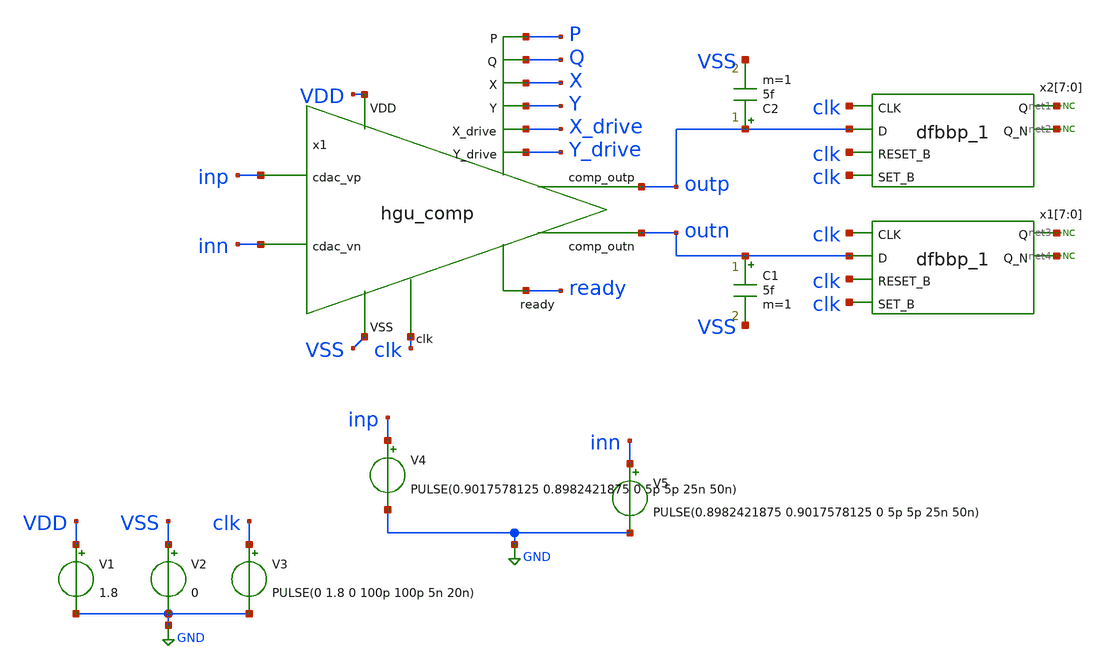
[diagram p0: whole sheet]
** sch_path: hgu/tb/tb_hgu_comp_withc.sch
**.subckt tb_hgu_comp_withc
x1 Y X X_drive P Q ready inn outp outn inp clk Y_drive VDD VSS hgu_comp
V1 VDD GND 1.8
V2 VSS GND 0
V3 clk GND PULSE(0 1.8 0 100p 100p 5n 20n)
V4 inp GND PULSE(0.9017578125 0.8982421875 0 5p 5p 25n 50n)
V5 inn GND PULSE(0.8982421875 0.9017578125 0 5p 5p 25n 50n)
x2[7] clk outp clk clk VGND VNB VPB VPWR net1 net2 sky130_fd_sc_hd__dfbbp_1
x2[6] clk outp clk clk VGND VNB VPB VPWR net1 net2 sky130_fd_sc_hd__dfbbp_1
x2[5] clk outp clk clk VGND VNB VPB VPWR net1 net2 sky130_fd_sc_hd__dfbbp_1
x2[4] clk outp clk clk VGND VNB VPB VPWR net1 net2 sky130_fd_sc_hd__dfbbp_1
x2[3] clk outp clk clk VGND VNB VPB VPWR net1 net2 sky130_fd_sc_hd__dfbbp_1
x2[2] clk outp clk clk VGND VNB VPB VPWR net1 net2 sky130_fd_sc_hd__dfbbp_1
x2[1] clk outp clk clk VGND VNB VPB VPWR net1 net2 sky130_fd_sc_hd__dfbbp_1
x2[0] clk outp clk clk VGND VNB VPB VPWR net1 net2 sky130_fd_sc_hd__dfbbp_1
x1[7] clk outn clk clk VGND VNB VPB VPWR net3 net4 sky130_fd_sc_hd__dfbbp_1
x1[6] clk outn clk clk VGND VNB VPB VPWR net3 net4 sky130_fd_sc_hd__dfbbp_1
x1[5] clk outn clk clk VGND VNB VPB VPWR net3 net4 sky130_fd_sc_hd__dfbbp_1
x1[4] clk outn clk clk VGND VNB VPB VPWR net3 net4 sky130_fd_sc_hd__dfbbp_1
x1[3] clk outn clk clk VGND VNB VPB VPWR net3 net4 sky130_fd_sc_hd__dfbbp_1
x1[2] clk outn clk clk VGND VNB VPB VPWR net3 net4 sky130_fd_sc_hd__dfbbp_1
x1[1] clk outn clk clk VGND VNB VPB VPWR net3 net4 sky130_fd_sc_hd__dfbbp_1
x1[0] clk outn clk clk VGND VNB VPB VPWR net3 net4 sky130_fd_sc_hd__dfbbp_1
C1 outn VSS 5f m=1
C2 outp VSS 5f m=1
* noconn #net1
* noconn #net2
* noconn #net3
* noconn #net4
**** begin user architecture code



.lib /foss/pdks/sky130A/libs.tech/ngspice/sky130.lib.spice tt
.include /foss/pdks/sky130A/libs.ref/sky130_fd_sc_hd/spice/sky130_fd_sc_hd.spice
.tran 1ns 100ns
.temp 100
.control
    run
     let svdd = 1.8
     let max = svdd*0.8
     let min = svdd*0.2
     let mid = svdd*0.5

   meas tran rising_s_d find time when V(clk)=mid RISE=1 TD=30n
   meas tran rising_e_d find time when V(outp)=mid RISE=1 TD=1000p
   let rising_delay = rising_e_d-rising_s_d

   meas tran falling_s_d find time when V(clk)=mid RISE=1 TD=50n
   meas tran falling_e_d find time when V(outp)=mid FALL=1 TD=50n
   let falling_delay = falling_e_d-falling_s_d

   meas tran rising_s find time when V(outp)=min RISE=1 TD=30n
      meas tran rising_e find time when V(outp)=max RISE=1 TD=30n
      let rising_time = rising_e-rising_s

      meas tran falling_s find time when V(outp)=max FALL=1 TD=50n
     meas tran falling_e find time when V(outp)=min FALL=1 TD=50n
      let falling_time = falling_e-falling_s

    print rising_time falling_time rising_delay falling_delay
    plot V(outp)+6 V(P)-2  V(X)+2  V(clk) V(inn) V(inp) V(Y)+2  V(outn)+6 V(Q)-2 V(ready)
+ V(X_drive)+4 V(Y_drive)+4
.endc
.save all


**** end user architecture code
**.ends

* expanding   symbol:  ../xschem/hgu_comp.sym # of pins=14
** sym_path: hgu/xschem/hgu_comp.sym
** sch_path: hgu/xschem/hgu_comp.sch
.subckt hgu_comp Y X X_drive P Q ready cdac_vn comp_outp comp_outn cdac_vp clk Y_drive VDD VSS
*.ipin cdac_vn
*.ipin cdac_vp
*.ipin VSS
*.ipin VDD
*.ipin clk
*.opin X
*.opin Y
*.opin P
*.opin Q
*.opin ready
*.opin X_drive
*.opin Y_drive
*.opin comp_outp
*.opin comp_outn
XM1 net1 clk VSS VSS sky130_fd_pr__nfet_01v8 L=0.15 W=4 nf=1 ad='int((nf+1)/2) * W/nf * 0.29' as='int((nf+2)/2) * W/nf * 0.29'
+ pd='2*int((nf+1)/2) * (W/nf + 0.29)' ps='2*int((nf+2)/2) * (W/nf + 0.29)' nrd='0.29 / W' nrs='0.29 / W'
+ sa=0 sb=0 sd=0 mult=1 m=1
XM4 Y X Q VSS sky130_fd_pr__nfet_01v8 L=0.15 W=4 nf=1 ad='int((nf+1)/2) * W/nf * 0.29' as='int((nf+2)/2) * W/nf * 0.29'
+ pd='2*int((nf+1)/2) * (W/nf + 0.29)' ps='2*int((nf+2)/2) * (W/nf + 0.29)' nrd='0.29 / W' nrs='0.29 / W'
+ sa=0 sb=0 sd=0 mult=1 m=1
XM5 X Y P VSS sky130_fd_pr__nfet_01v8 L=0.15 W=4 nf=1 ad='int((nf+1)/2) * W/nf * 0.29' as='int((nf+2)/2) * W/nf * 0.29'
+ pd='2*int((nf+1)/2) * (W/nf + 0.29)' ps='2*int((nf+2)/2) * (W/nf + 0.29)' nrd='0.29 / W' nrs='0.29 / W'
+ sa=0 sb=0 sd=0 mult=1 m=1
XM6 X Y VDD VDD sky130_fd_pr__pfet_01v8 L=0.15 W=2 nf=1 ad='int((nf+1)/2) * W/nf * 0.29' as='int((nf+2)/2) * W/nf * 0.29'
+ pd='2*int((nf+1)/2) * (W/nf + 0.29)' ps='2*int((nf+2)/2) * (W/nf + 0.29)' nrd='0.29 / W' nrs='0.29 / W'
+ sa=0 sb=0 sd=0 mult=1 m=1
XM7 Y X VDD VDD sky130_fd_pr__pfet_01v8 L=0.15 W=2 nf=1 ad='int((nf+1)/2) * W/nf * 0.29' as='int((nf+2)/2) * W/nf * 0.29'
+ pd='2*int((nf+1)/2) * (W/nf + 0.29)' ps='2*int((nf+2)/2) * (W/nf + 0.29)' nrd='0.29 / W' nrs='0.29 / W'
+ sa=0 sb=0 sd=0 mult=1 m=1
XM8 X clk VDD VDD sky130_fd_pr__pfet_01v8 L=0.15 W=2 nf=1 ad='int((nf+1)/2) * W/nf * 0.29' as='int((nf+2)/2) * W/nf * 0.29'
+ pd='2*int((nf+1)/2) * (W/nf + 0.29)' ps='2*int((nf+2)/2) * (W/nf + 0.29)' nrd='0.29 / W' nrs='0.29 / W'
+ sa=0 sb=0 sd=0 mult=1 m=1
XM9 P clk VDD VDD sky130_fd_pr__pfet_01v8 L=0.15 W=2 nf=1 ad='int((nf+1)/2) * W/nf * 0.29' as='int((nf+2)/2) * W/nf * 0.29'
+ pd='2*int((nf+1)/2) * (W/nf + 0.29)' ps='2*int((nf+2)/2) * (W/nf + 0.29)' nrd='0.29 / W' nrs='0.29 / W'
+ sa=0 sb=0 sd=0 mult=1 m=1
XM10 Y clk VDD VDD sky130_fd_pr__pfet_01v8 L=0.15 W=2 nf=1 ad='int((nf+1)/2) * W/nf * 0.29' as='int((nf+2)/2) * W/nf * 0.29'
+ pd='2*int((nf+1)/2) * (W/nf + 0.29)' ps='2*int((nf+2)/2) * (W/nf + 0.29)' nrd='0.29 / W' nrs='0.29 / W'
+ sa=0 sb=0 sd=0 mult=1 m=1
XM11 Q clk VDD VDD sky130_fd_pr__pfet_01v8 L=0.15 W=2 nf=1 ad='int((nf+1)/2) * W/nf * 0.29' as='int((nf+2)/2) * W/nf * 0.29'
+ pd='2*int((nf+1)/2) * (W/nf + 0.29)' ps='2*int((nf+2)/2) * (W/nf + 0.29)' nrd='0.29 / W' nrs='0.29 / W'
+ sa=0 sb=0 sd=0 mult=1 m=1
XM16 RS_n RS_p VDD VDD sky130_fd_pr__pfet_01v8 L=0.15 W=0.84 nf=1 ad='int((nf+1)/2) * W/nf * 0.29' as='int((nf+2)/2) * W/nf * 0.29'
+ pd='2*int((nf+1)/2) * (W/nf + 0.29)' ps='2*int((nf+2)/2) * (W/nf + 0.29)' nrd='0.29 / W' nrs='0.29 / W'
+ sa=0 sb=0 sd=0 mult=1 m=1
XM17 RS_p RS_n VDD VDD sky130_fd_pr__pfet_01v8 L=0.15 W=0.84 nf=1 ad='int((nf+1)/2) * W/nf * 0.29' as='int((nf+2)/2) * W/nf * 0.29'
+ pd='2*int((nf+1)/2) * (W/nf + 0.29)' ps='2*int((nf+2)/2) * (W/nf + 0.29)' nrd='0.29 / W' nrs='0.29 / W'
+ sa=0 sb=0 sd=0 mult=1 m=1
XM19 RS_p Y_inv VSS VSS sky130_fd_pr__nfet_01v8 L=0.15 W=0.84 nf=1 ad='int((nf+1)/2) * W/nf * 0.29' as='int((nf+2)/2) * W/nf * 0.29'
+ pd='2*int((nf+1)/2) * (W/nf + 0.29)' ps='2*int((nf+2)/2) * (W/nf + 0.29)' nrd='0.29 / W' nrs='0.29 / W'
+ sa=0 sb=0 sd=0 mult=1 m=1
XM23 RS_n X_inv VSS VSS sky130_fd_pr__nfet_01v8 L=0.15 W=0.84 nf=1 ad='int((nf+1)/2) * W/nf * 0.29' as='int((nf+2)/2) * W/nf * 0.29'
+ pd='2*int((nf+1)/2) * (W/nf + 0.29)' ps='2*int((nf+2)/2) * (W/nf + 0.29)' nrd='0.29 / W' nrs='0.29 / W'
+ sa=0 sb=0 sd=0 mult=1 m=1
XM2 P cdac_vp net1 VSS sky130_fd_pr__nfet_01v8_lvt L=0.15 W=8 nf=4 ad='int((nf+1)/2) * W / nf * 0.29'
+ as='int((nf+2)/2) * W / nf * 0.29' pd='2*int((nf+1)/2) * (W / nf + 0.29)' ps='2*int((nf+2)/2) * (W / nf + 0.29)'
+ nrd='0.29 / W ' nrs='0.29 / W ' sa=0 sb=0 sd=0 mult=1 m=1
XM3 Q cdac_vn net1 VSS sky130_fd_pr__nfet_01v8_lvt L=0.15 W=8 nf=4 ad='int((nf+1)/2) * W / nf * 0.29'
+ as='int((nf+2)/2) * W / nf * 0.29' pd='2*int((nf+1)/2) * (W / nf + 0.29)' ps='2*int((nf+2)/2) * (W / nf + 0.29)'
+ nrd='0.29 / W ' nrs='0.29 / W ' sa=0 sb=0 sd=0 mult=1 m=1
XM12 X_inv X VDD VDD sky130_fd_pr__pfet_01v8 L=0.15 W=0.84 nf=1 ad='int((nf+1)/2) * W/nf * 0.29' as='int((nf+2)/2) * W/nf * 0.29'
+ pd='2*int((nf+1)/2) * (W/nf + 0.29)' ps='2*int((nf+2)/2) * (W/nf + 0.29)' nrd='0.29 / W' nrs='0.29 / W'
+ sa=0 sb=0 sd=0 mult=1 m=1
XM13 X_inv X VSS VSS sky130_fd_pr__nfet_01v8 L=0.15 W=0.42 nf=1 ad='int((nf+1)/2) * W/nf * 0.29' as='int((nf+2)/2) * W/nf * 0.29'
+ pd='2*int((nf+1)/2) * (W/nf + 0.29)' ps='2*int((nf+2)/2) * (W/nf + 0.29)' nrd='0.29 / W' nrs='0.29 / W'
+ sa=0 sb=0 sd=0 mult=1 m=1
XM14 X_drive X_inv VDD VDD sky130_fd_pr__pfet_01v8 L=0.15 W=2 nf=3 ad='int((nf+1)/2) * W/nf * 0.29' as='int((nf+2)/2) * W/nf * 0.29'
+ pd='2*int((nf+1)/2) * (W/nf + 0.29)' ps='2*int((nf+2)/2) * (W/nf + 0.29)' nrd='0.29 / W' nrs='0.29 / W'
+ sa=0 sb=0 sd=0 mult=1 m=1
XM15 X_drive X_inv VSS VSS sky130_fd_pr__nfet_01v8 L=0.15 W=1 nf=1 ad='int((nf+1)/2) * W/nf * 0.29' as='int((nf+2)/2) * W/nf * 0.29'
+ pd='2*int((nf+1)/2) * (W/nf + 0.29)' ps='2*int((nf+2)/2) * (W/nf + 0.29)' nrd='0.29 / W' nrs='0.29 / W'
+ sa=0 sb=0 sd=0 mult=1 m=1
XM18 Y_inv Y VDD VDD sky130_fd_pr__pfet_01v8 L=0.15 W=0.84 nf=1 ad='int((nf+1)/2) * W/nf * 0.29' as='int((nf+2)/2) * W/nf * 0.29'
+ pd='2*int((nf+1)/2) * (W/nf + 0.29)' ps='2*int((nf+2)/2) * (W/nf + 0.29)' nrd='0.29 / W' nrs='0.29 / W'
+ sa=0 sb=0 sd=0 mult=1 m=1
XM20 Y_inv Y VSS VSS sky130_fd_pr__nfet_01v8 L=0.15 W=0.42 nf=1 ad='int((nf+1)/2) * W/nf * 0.29' as='int((nf+2)/2) * W/nf * 0.29'
+ pd='2*int((nf+1)/2) * (W/nf + 0.29)' ps='2*int((nf+2)/2) * (W/nf + 0.29)' nrd='0.29 / W' nrs='0.29 / W'
+ sa=0 sb=0 sd=0 mult=1 m=1
XM21 Y_drive Y_inv VDD VDD sky130_fd_pr__pfet_01v8 L=0.15 W=2 nf=3 ad='int((nf+1)/2) * W/nf * 0.29' as='int((nf+2)/2) * W/nf * 0.29'
+ pd='2*int((nf+1)/2) * (W/nf + 0.29)' ps='2*int((nf+2)/2) * (W/nf + 0.29)' nrd='0.29 / W' nrs='0.29 / W'
+ sa=0 sb=0 sd=0 mult=1 m=1
XM22 Y_drive Y_inv VSS VSS sky130_fd_pr__nfet_01v8 L=0.15 W=1 nf=1 ad='int((nf+1)/2) * W/nf * 0.29' as='int((nf+2)/2) * W/nf * 0.29'
+ pd='2*int((nf+1)/2) * (W/nf + 0.29)' ps='2*int((nf+2)/2) * (W/nf + 0.29)' nrd='0.29 / W' nrs='0.29 / W'
+ sa=0 sb=0 sd=0 mult=1 m=1
XM24 net2 Y_drive X_drive VDD sky130_fd_pr__pfet_01v8 L=0.15 W=0.84 nf=1 ad='int((nf+1)/2) * W/nf * 0.29'
+ as='int((nf+2)/2) * W/nf * 0.29' pd='2*int((nf+1)/2) * (W/nf + 0.29)' ps='2*int((nf+2)/2) * (W/nf + 0.29)'
+ nrd='0.29 / W' nrs='0.29 / W' sa=0 sb=0 sd=0 mult=1 m=1
XM25 net2 X_drive Y_drive VDD sky130_fd_pr__pfet_01v8 L=0.15 W=0.84 nf=1 ad='int((nf+1)/2) * W/nf * 0.29'
+ as='int((nf+2)/2) * W/nf * 0.29' pd='2*int((nf+1)/2) * (W/nf + 0.29)' ps='2*int((nf+2)/2) * (W/nf + 0.29)'
+ nrd='0.29 / W' nrs='0.29 / W' sa=0 sb=0 sd=0 mult=1 m=1
XM26 net2 Y_drive net3 VSS sky130_fd_pr__nfet_01v8 L=0.15 W=0.84 nf=1 ad='int((nf+1)/2) * W/nf * 0.29'
+ as='int((nf+2)/2) * W/nf * 0.29' pd='2*int((nf+1)/2) * (W/nf + 0.29)' ps='2*int((nf+2)/2) * (W/nf + 0.29)'
+ nrd='0.29 / W' nrs='0.29 / W' sa=0 sb=0 sd=0 mult=1 m=1
XM27 net3 X_drive VSS VSS sky130_fd_pr__nfet_01v8 L=0.15 W=0.84 nf=1 ad='int((nf+1)/2) * W/nf * 0.29'
+ as='int((nf+2)/2) * W/nf * 0.29' pd='2*int((nf+1)/2) * (W/nf + 0.29)' ps='2*int((nf+2)/2) * (W/nf + 0.29)'
+ nrd='0.29 / W' nrs='0.29 / W' sa=0 sb=0 sd=0 mult=1 m=1
XM28 ready net2 VDD VDD sky130_fd_pr__pfet_01v8 L=0.15 W=0.84 nf=1 ad='int((nf+1)/2) * W/nf * 0.29' as='int((nf+2)/2) * W/nf * 0.29'
+ pd='2*int((nf+1)/2) * (W/nf + 0.29)' ps='2*int((nf+2)/2) * (W/nf + 0.29)' nrd='0.29 / W' nrs='0.29 / W'
+ sa=0 sb=0 sd=0 mult=1 m=1
XM29 ready net2 VSS VSS sky130_fd_pr__nfet_01v8 L=0.15 W=0.42 nf=1 ad='int((nf+1)/2) * W/nf * 0.29' as='int((nf+2)/2) * W/nf * 0.29'
+ pd='2*int((nf+1)/2) * (W/nf + 0.29)' ps='2*int((nf+2)/2) * (W/nf + 0.29)' nrd='0.29 / W' nrs='0.29 / W'
+ sa=0 sb=0 sd=0 mult=1 m=1
C1 Q VSS 5f m=1
C2 P VSS 5f m=1
C3 Y VSS 5f m=1
C4 X VSS 5f m=1
C5 net1 VSS 5f m=1
C6 cdac_vn VSS 5f m=1
C7 cdac_vp VSS 5f m=1
C8 X_inv VSS 5f m=1
C9 Y_inv VSS 5f m=1
C10 Y_drive VSS 5f m=1
C11 X_drive VSS 5f m=1
C12 net2 VSS 5f m=1
C13 ready VSS 5f m=1
C14 RS_p VSS 5f m=1
C15 RS_n VSS 5f m=1
C16 clk VSS 5f m=1
C17 clk VSS 5f m=1
C18 clk VSS 5f m=1
C19 clk VSS 5f m=1
C20 clk VSS 5f m=1
XM30 net4 RS_p VDD VDD sky130_fd_pr__pfet_01v8 L=0.15 W=0.84 nf=1 ad='int((nf+1)/2) * W/nf * 0.29' as='int((nf+2)/2) * W/nf * 0.29'
+ pd='2*int((nf+1)/2) * (W/nf + 0.29)' ps='2*int((nf+2)/2) * (W/nf + 0.29)' nrd='0.29 / W' nrs='0.29 / W'
+ sa=0 sb=0 sd=0 mult=1 m=1
XM31 net4 RS_p VSS VSS sky130_fd_pr__nfet_01v8 L=0.15 W=0.42 nf=1 ad='int((nf+1)/2) * W/nf * 0.29' as='int((nf+2)/2) * W/nf * 0.29'
+ pd='2*int((nf+1)/2) * (W/nf + 0.29)' ps='2*int((nf+2)/2) * (W/nf + 0.29)' nrd='0.29 / W' nrs='0.29 / W'
+ sa=0 sb=0 sd=0 mult=1 m=1
XM32 comp_outp net4 VDD VDD sky130_fd_pr__pfet_01v8 L=0.15 W=2 nf=3 ad='int((nf+1)/2) * W/nf * 0.29'
+ as='int((nf+2)/2) * W/nf * 0.29' pd='2*int((nf+1)/2) * (W/nf + 0.29)' ps='2*int((nf+2)/2) * (W/nf + 0.29)'
+ nrd='0.29 / W' nrs='0.29 / W' sa=0 sb=0 sd=0 mult=1 m=1
XM33 comp_outp net4 VSS VSS sky130_fd_pr__nfet_01v8 L=0.15 W=1 nf=1 ad='int((nf+1)/2) * W/nf * 0.29'
+ as='int((nf+2)/2) * W/nf * 0.29' pd='2*int((nf+1)/2) * (W/nf + 0.29)' ps='2*int((nf+2)/2) * (W/nf + 0.29)'
+ nrd='0.29 / W' nrs='0.29 / W' sa=0 sb=0 sd=0 mult=1 m=1
XM34 net5 RS_n VDD VDD sky130_fd_pr__pfet_01v8 L=0.15 W=0.84 nf=1 ad='int((nf+1)/2) * W/nf * 0.29' as='int((nf+2)/2) * W/nf * 0.29'
+ pd='2*int((nf+1)/2) * (W/nf + 0.29)' ps='2*int((nf+2)/2) * (W/nf + 0.29)' nrd='0.29 / W' nrs='0.29 / W'
+ sa=0 sb=0 sd=0 mult=1 m=1
XM35 net5 RS_n VSS VSS sky130_fd_pr__nfet_01v8 L=0.15 W=0.42 nf=1 ad='int((nf+1)/2) * W/nf * 0.29' as='int((nf+2)/2) * W/nf * 0.29'
+ pd='2*int((nf+1)/2) * (W/nf + 0.29)' ps='2*int((nf+2)/2) * (W/nf + 0.29)' nrd='0.29 / W' nrs='0.29 / W'
+ sa=0 sb=0 sd=0 mult=1 m=1
XM36 comp_outn net5 VDD VDD sky130_fd_pr__pfet_01v8 L=0.15 W=2 nf=3 ad='int((nf+1)/2) * W/nf * 0.29'
+ as='int((nf+2)/2) * W/nf * 0.29' pd='2*int((nf+1)/2) * (W/nf + 0.29)' ps='2*int((nf+2)/2) * (W/nf + 0.29)'
+ nrd='0.29 / W' nrs='0.29 / W' sa=0 sb=0 sd=0 mult=1 m=1
XM37 comp_outn net5 VSS VSS sky130_fd_pr__nfet_01v8 L=0.15 W=1 nf=1 ad='int((nf+1)/2) * W/nf * 0.29'
+ as='int((nf+2)/2) * W/nf * 0.29' pd='2*int((nf+1)/2) * (W/nf + 0.29)' ps='2*int((nf+2)/2) * (W/nf + 0.29)'
+ nrd='0.29 / W' nrs='0.29 / W' sa=0 sb=0 sd=0 mult=1 m=1
C21 net4 VSS 5f m=1
C22 net5 VSS 5f m=1
C23 comp_outn VSS 5f m=1
C24 comp_outp VSS 5f m=1
.ends

.GLOBAL GND
.end
